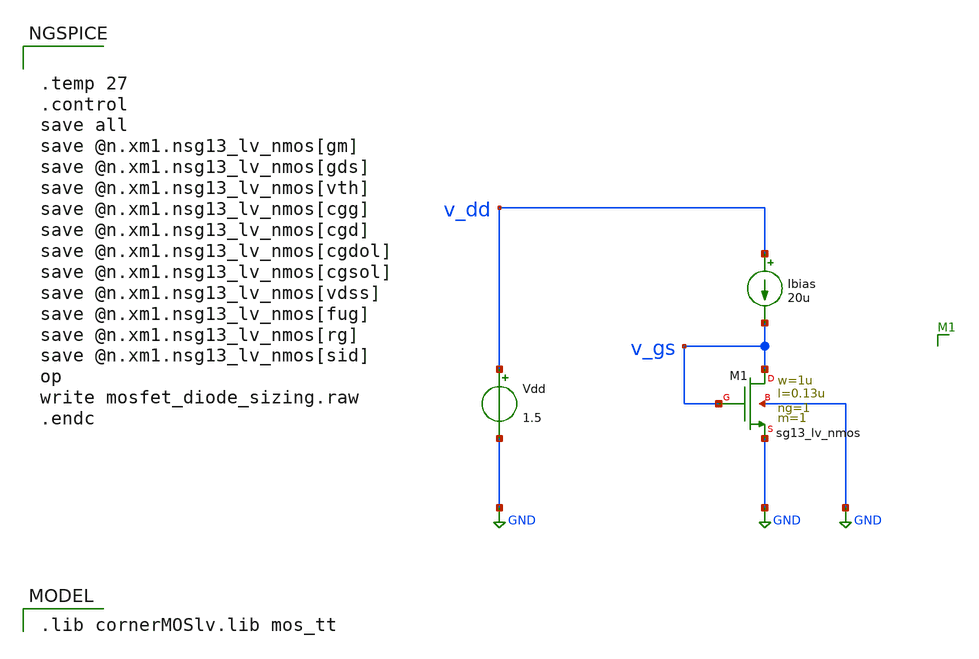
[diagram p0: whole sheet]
** sch_path: xschem/mosfet_diode_sizing.sch
* (c) 2024 H. Pretl, Apache-2.0 license
**.subckt mosfet_diode_sizing
Vdd v_dd GND 1.5
XM1 v_gs v_gs GND GND sg13_lv_nmos w=1u l=0.13u ng=1 m=1 mm_ok=1
Ibias v_dd v_gs 20u
**** begin user architecture code
 .lib cornerMOSlv.lib mos_tt



.temp 27
.control
save all
save @n.xm1.nsg13_lv_nmos[gm]
save @n.xm1.nsg13_lv_nmos[gds]
save @n.xm1.nsg13_lv_nmos[vth]
save @n.xm1.nsg13_lv_nmos[cgg]
save @n.xm1.nsg13_lv_nmos[cgd]
save @n.xm1.nsg13_lv_nmos[cgdol]
save @n.xm1.nsg13_lv_nmos[cgsol]
save @n.xm1.nsg13_lv_nmos[vdss]
save @n.xm1.nsg13_lv_nmos[fug]
save @n.xm1.nsg13_lv_nmos[rg]
save @n.xm1.nsg13_lv_nmos[sid]
op
write mosfet_diode_sizing.raw
.endc


**** end user architecture code
**.ends
.GLOBAL GND
.end
